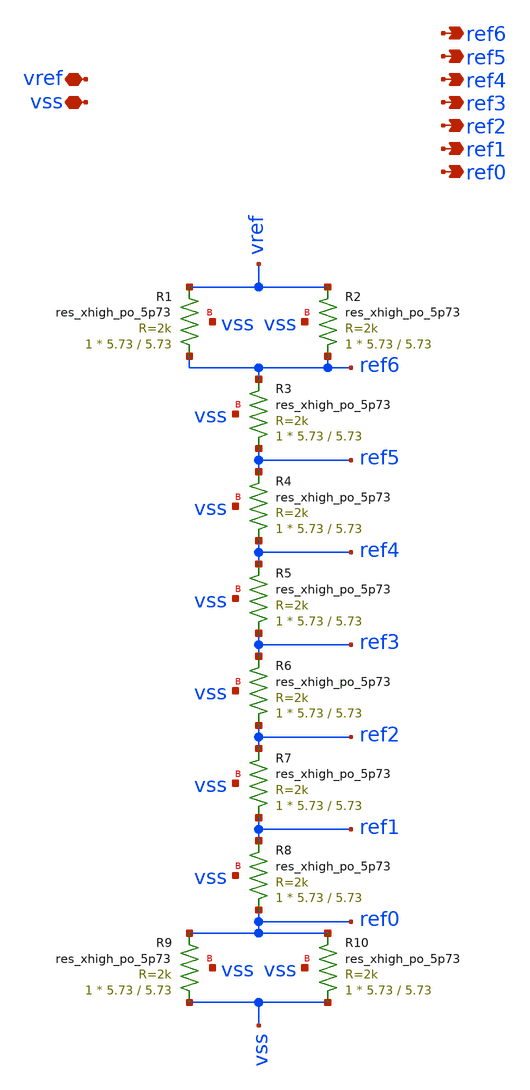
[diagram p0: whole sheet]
** sch_path: xsch/ip/res_ladder_vref/res_ladder_vref.sch
**.subckt res_ladder_vref vref vss ref0 ref1 ref2 ref3 ref4 ref5 ref6
*.iopin vref
*.iopin vss
*.opin ref0
*.opin ref1
*.opin ref2
*.opin ref3
*.opin ref4
*.opin ref5
*.opin ref6
XR1 ref6 vref vss sky130_fd_pr__res_xhigh_po_5p73 L=5.73 mult=1 m=1
XR2 ref6 vref vss sky130_fd_pr__res_xhigh_po_5p73 L=5.73 mult=1 m=1
XR3 ref5 ref6 vss sky130_fd_pr__res_xhigh_po_5p73 L=5.73 mult=1 m=1
XR4 ref4 ref5 vss sky130_fd_pr__res_xhigh_po_5p73 L=5.73 mult=1 m=1
XR5 ref3 ref4 vss sky130_fd_pr__res_xhigh_po_5p73 L=5.73 mult=1 m=1
XR6 ref2 ref3 vss sky130_fd_pr__res_xhigh_po_5p73 L=5.73 mult=1 m=1
XR7 ref1 ref2 vss sky130_fd_pr__res_xhigh_po_5p73 L=5.73 mult=1 m=1
XR8 ref0 ref1 vss sky130_fd_pr__res_xhigh_po_5p73 L=5.73 mult=1 m=1
XR9 vss ref0 vss sky130_fd_pr__res_xhigh_po_5p73 L=5.73 mult=1 m=1
XR10 vss ref0 vss sky130_fd_pr__res_xhigh_po_5p73 L=5.73 mult=1 m=1
**.ends
.end
